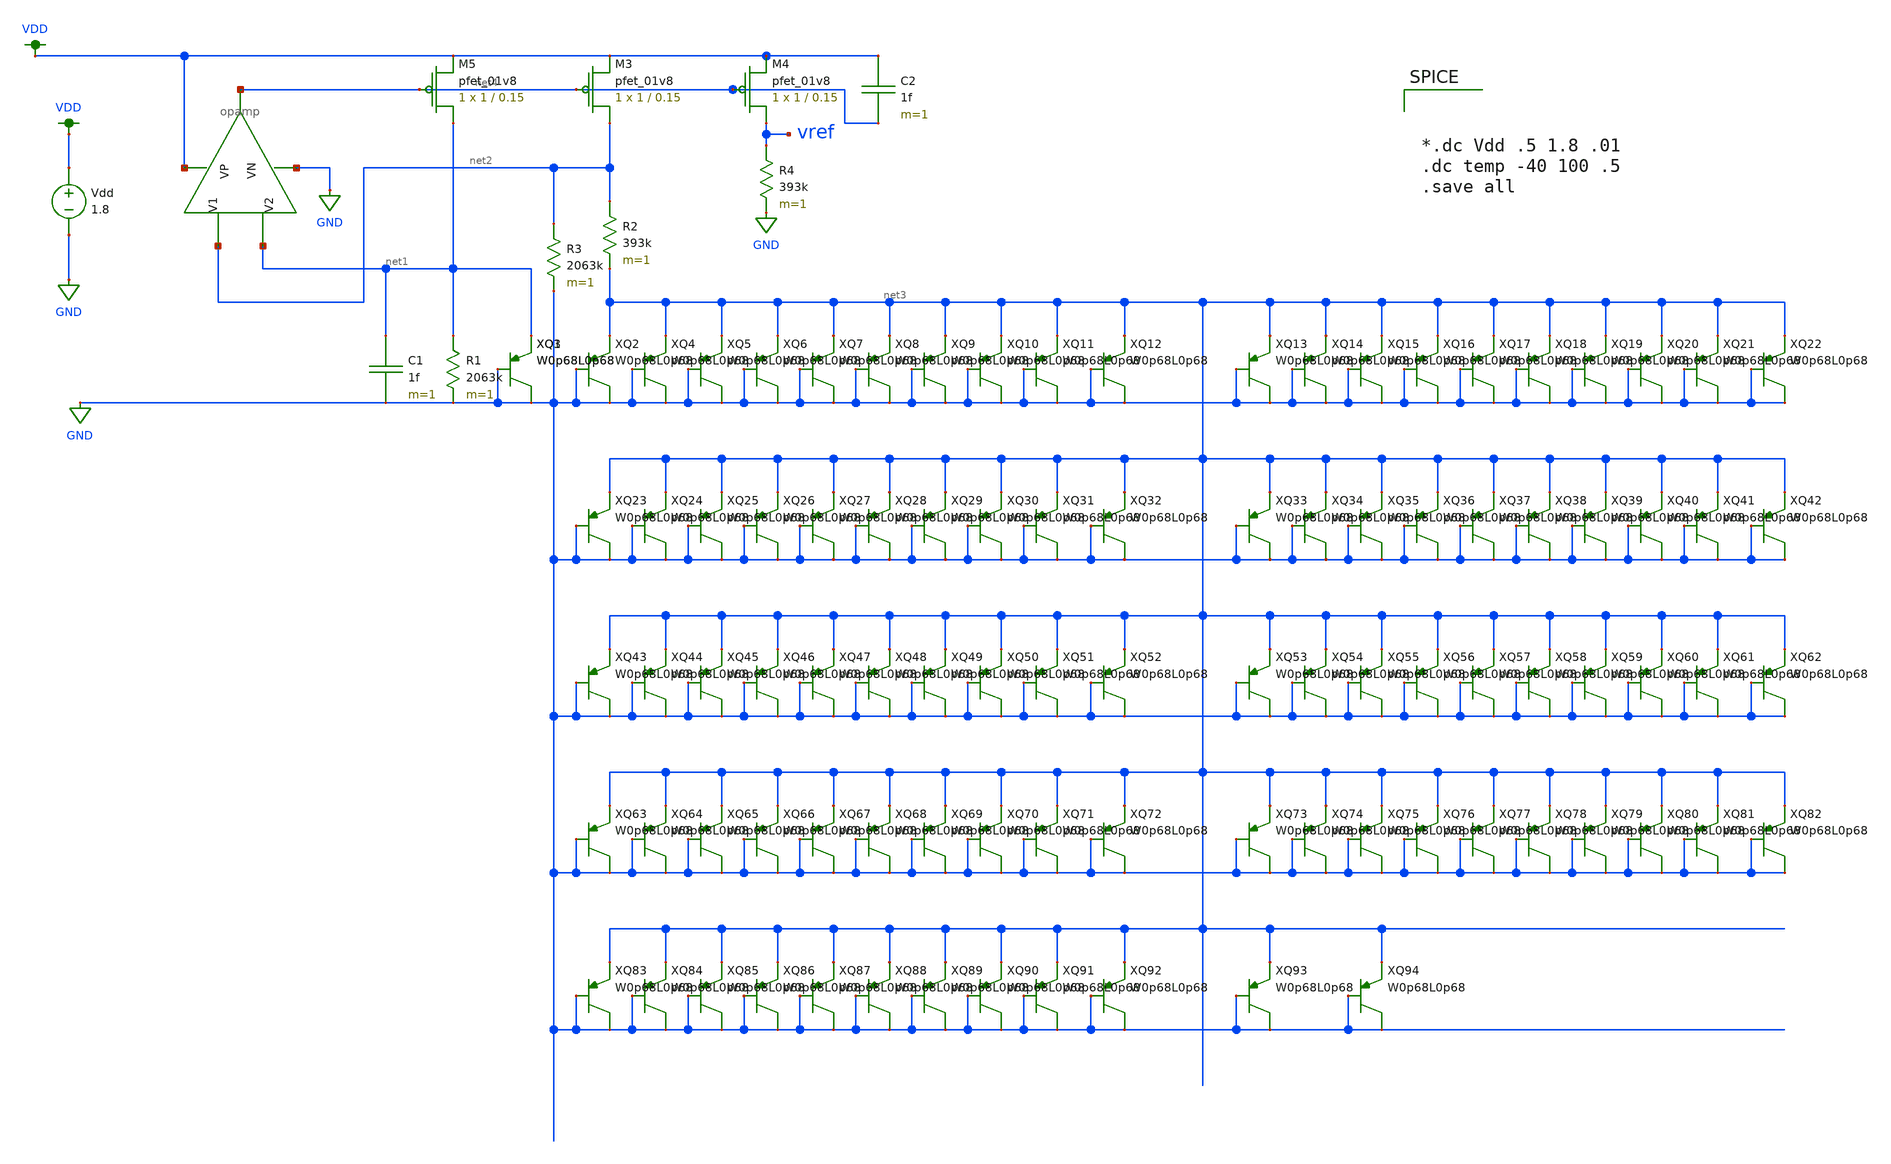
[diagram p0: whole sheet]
** sch_path: schematics/bandgap_pnp.sch
**.subckt bandgap_pnp
XM4 vref net4 VDD VDD sky130_fd_pr__pfet_01v8 L=0.15 W=1 nf=1 ad='int((nf+1)/2) * W/nf * 0.29' as='int((nf+2)/2) * W/nf * 0.29'
+ pd='2*int((nf+1)/2) * (W/nf + 0.29)' ps='2*int((nf+2)/2) * (W/nf + 0.29)' nrd='0.29 / W' nrs='0.29 / W'
+ sa=0 sb=0 sd=0 mult=1 m=1
XM5 net1 net4 VDD VDD sky130_fd_pr__pfet_01v8 L=0.15 W=1 nf=1 ad='int((nf+1)/2) * W/nf * 0.29' as='int((nf+2)/2) * W/nf * 0.29'
+ pd='2*int((nf+1)/2) * (W/nf + 0.29)' ps='2*int((nf+2)/2) * (W/nf + 0.29)' nrd='0.29 / W' nrs='0.29 / W'
+ sa=0 sb=0 sd=0 mult=1 m=1
XM3 net2 net4 VDD VDD sky130_fd_pr__pfet_01v8 L=0.15 W=1 nf=1 ad='int((nf+1)/2) * W/nf * 0.29' as='int((nf+2)/2) * W/nf * 0.29'
+ pd='2*int((nf+1)/2) * (W/nf + 0.29)' ps='2*int((nf+2)/2) * (W/nf + 0.29)' nrd='0.29 / W' nrs='0.29 / W'
+ sa=0 sb=0 sd=0 mult=1 m=1
C1 net1 GND 1f m=1
R1 net1 GND 2063k m=1
R2 net2 net3 393k m=1
R3 net2 GND 2063k m=1
R4 vref GND 393k m=1
C2 VDD net4 1f m=1
Vdd VDD GND 1.8
X1 net2 net1 VDD GND net4 opamp
XQ1 net1 GND GND sky130_fd_pr__pnp_05v0
XQ2 net3 GND GND sky130_fd_pr__pnp_05v0
XQ3 net1 GND GND sky130_fd_pr__pnp_05v0
XQ4 net3 GND GND sky130_fd_pr__pnp_05v0
XQ5 net3 GND GND sky130_fd_pr__pnp_05v0
XQ6 net3 GND GND sky130_fd_pr__pnp_05v0
XQ7 net3 GND GND sky130_fd_pr__pnp_05v0
XQ8 net3 GND GND sky130_fd_pr__pnp_05v0
XQ9 net3 GND GND sky130_fd_pr__pnp_05v0
XQ10 net3 GND GND sky130_fd_pr__pnp_05v0
XQ11 net3 GND GND sky130_fd_pr__pnp_05v0
XQ12 net3 GND GND sky130_fd_pr__pnp_05v0
XQ13 net3 GND GND sky130_fd_pr__pnp_05v0
XQ14 net3 GND GND sky130_fd_pr__pnp_05v0
XQ15 net3 GND GND sky130_fd_pr__pnp_05v0
XQ16 net3 GND GND sky130_fd_pr__pnp_05v0
XQ17 net3 GND GND sky130_fd_pr__pnp_05v0
XQ18 net3 GND GND sky130_fd_pr__pnp_05v0
XQ19 net3 GND GND sky130_fd_pr__pnp_05v0
XQ20 net3 GND GND sky130_fd_pr__pnp_05v0
XQ21 net3 GND GND sky130_fd_pr__pnp_05v0
XQ22 net3 GND GND sky130_fd_pr__pnp_05v0
XQ23 net3 GND GND sky130_fd_pr__pnp_05v0
XQ24 net3 GND GND sky130_fd_pr__pnp_05v0
XQ25 net3 GND GND sky130_fd_pr__pnp_05v0
XQ26 net3 GND GND sky130_fd_pr__pnp_05v0
XQ27 net3 GND GND sky130_fd_pr__pnp_05v0
XQ28 net3 GND GND sky130_fd_pr__pnp_05v0
XQ29 net3 GND GND sky130_fd_pr__pnp_05v0
XQ30 net3 GND GND sky130_fd_pr__pnp_05v0
XQ31 net3 GND GND sky130_fd_pr__pnp_05v0
XQ32 net3 GND GND sky130_fd_pr__pnp_05v0
XQ33 net3 GND GND sky130_fd_pr__pnp_05v0
XQ34 net3 GND GND sky130_fd_pr__pnp_05v0
XQ35 net3 GND GND sky130_fd_pr__pnp_05v0
XQ36 net3 GND GND sky130_fd_pr__pnp_05v0
XQ37 net3 GND GND sky130_fd_pr__pnp_05v0
XQ38 net3 GND GND sky130_fd_pr__pnp_05v0
XQ39 net3 GND GND sky130_fd_pr__pnp_05v0
XQ40 net3 GND GND sky130_fd_pr__pnp_05v0
XQ41 net3 GND GND sky130_fd_pr__pnp_05v0
XQ42 net3 GND GND sky130_fd_pr__pnp_05v0
XQ43 net3 GND GND sky130_fd_pr__pnp_05v0
XQ44 net3 GND GND sky130_fd_pr__pnp_05v0
XQ45 net3 GND GND sky130_fd_pr__pnp_05v0
XQ46 net3 GND GND sky130_fd_pr__pnp_05v0
XQ47 net3 GND GND sky130_fd_pr__pnp_05v0
XQ48 net3 GND GND sky130_fd_pr__pnp_05v0
XQ49 net3 GND GND sky130_fd_pr__pnp_05v0
XQ50 net3 GND GND sky130_fd_pr__pnp_05v0
XQ51 net3 GND GND sky130_fd_pr__pnp_05v0
XQ52 net3 GND GND sky130_fd_pr__pnp_05v0
XQ53 net3 GND GND sky130_fd_pr__pnp_05v0
XQ54 net3 GND GND sky130_fd_pr__pnp_05v0
XQ55 net3 GND GND sky130_fd_pr__pnp_05v0
XQ56 net3 GND GND sky130_fd_pr__pnp_05v0
XQ57 net3 GND GND sky130_fd_pr__pnp_05v0
XQ58 net3 GND GND sky130_fd_pr__pnp_05v0
XQ59 net3 GND GND sky130_fd_pr__pnp_05v0
XQ60 net3 GND GND sky130_fd_pr__pnp_05v0
XQ61 net3 GND GND sky130_fd_pr__pnp_05v0
XQ62 net3 GND GND sky130_fd_pr__pnp_05v0
XQ63 net3 GND GND sky130_fd_pr__pnp_05v0
XQ64 net3 GND GND sky130_fd_pr__pnp_05v0
XQ65 net3 GND GND sky130_fd_pr__pnp_05v0
XQ66 net3 GND GND sky130_fd_pr__pnp_05v0
XQ67 net3 GND GND sky130_fd_pr__pnp_05v0
XQ68 net3 GND GND sky130_fd_pr__pnp_05v0
XQ69 net3 GND GND sky130_fd_pr__pnp_05v0
XQ70 net3 GND GND sky130_fd_pr__pnp_05v0
XQ71 net3 GND GND sky130_fd_pr__pnp_05v0
XQ72 net3 GND GND sky130_fd_pr__pnp_05v0
XQ73 net3 GND GND sky130_fd_pr__pnp_05v0
XQ74 net3 GND GND sky130_fd_pr__pnp_05v0
XQ75 net3 GND GND sky130_fd_pr__pnp_05v0
XQ76 net3 GND GND sky130_fd_pr__pnp_05v0
XQ77 net3 GND GND sky130_fd_pr__pnp_05v0
XQ78 net3 GND GND sky130_fd_pr__pnp_05v0
XQ79 net3 GND GND sky130_fd_pr__pnp_05v0
XQ80 net3 GND GND sky130_fd_pr__pnp_05v0
XQ81 net3 GND GND sky130_fd_pr__pnp_05v0
XQ82 net3 GND GND sky130_fd_pr__pnp_05v0
XQ83 net3 GND GND sky130_fd_pr__pnp_05v0
XQ84 net3 GND GND sky130_fd_pr__pnp_05v0
XQ85 net3 GND GND sky130_fd_pr__pnp_05v0
XQ86 net3 GND GND sky130_fd_pr__pnp_05v0
XQ87 net3 GND GND sky130_fd_pr__pnp_05v0
XQ88 net3 GND GND sky130_fd_pr__pnp_05v0
XQ89 net3 GND GND sky130_fd_pr__pnp_05v0
XQ90 net3 GND GND sky130_fd_pr__pnp_05v0
XQ91 net3 GND GND sky130_fd_pr__pnp_05v0
XQ92 net3 GND GND sky130_fd_pr__pnp_05v0
XQ93 net3 GND GND sky130_fd_pr__pnp_05v0
XQ94 net3 GND GND sky130_fd_pr__pnp_05v0
**** begin user architecture code

.option wnflag=1
.param MC_SWITCH=0.0
.lib ~/skywater/skywater-pdk/libraries/sky130_fd_pr_ngspice/latest/models/sky130.lib.spice tt




*.dc Vdd .5 1.8 .01
.dc temp -40 100 .5
.save all




.subckt sky130_fd_pr__pnp_05v0  E B C
*.iopin E
*.iopin B
*.iopin C
XQ1 C B E C sky130_fd_pr__pnp_05v5_W0p68L0p68
.ends

**** end user architecture code
**.ends

* expanding   symbol:  /home/madvlsi/Desktop/MADVLSI_final/schematics/opamp.sym # of pins=5
** sym_path: schematics/opamp.sym
** sch_path: schematics/opamp.sch
.subckt opamp V1 V2 VP VN Vout
*.ipin V1
*.ipin V2
*.opin Vout
*.iopin VP
*.iopin VN
*.iopin VP
*.iopin VN
XM1 VN net7 net2 GND sky130_fd_pr__nfet_01v8 L=l W=w nf=1 ad='int((nf+1)/2) * W/nf * 0.29' as='int((nf+2)/2) * W/nf * 0.29'
+ pd='2*int((nf+1)/2) * (W/nf + 0.29)' ps='2*int((nf+2)/2) * (W/nf + 0.29)' nrd='0.29 / W' nrs='0.29 / W'
+ sa=0 sb=0 sd=0 mult=1 m=1
XM2 VP net3 net1 VDD sky130_fd_pr__pfet_01v8 L=l W=w nf=1 ad='int((nf+1)/2) * W/nf * 0.29' as='int((nf+2)/2) * W/nf * 0.29'
+ pd='2*int((nf+1)/2) * (W/nf + 0.29)' ps='2*int((nf+2)/2) * (W/nf + 0.29)' nrd='0.29 / W' nrs='0.29 / W'
+ sa=0 sb=0 sd=0 mult=1 m=1
XM3 net1 V1 Vd VDD sky130_fd_pr__pfet_01v8 L=l W=w nf=1 ad='int((nf+1)/2) * W/nf * 0.29' as='int((nf+2)/2) * W/nf * 0.29'
+ pd='2*int((nf+1)/2) * (W/nf + 0.29)' ps='2*int((nf+2)/2) * (W/nf + 0.29)' nrd='0.29 / W' nrs='0.29 / W'
+ sa=0 sb=0 sd=0 mult=1 m=1
XM4 Vc V2 net1 VDD sky130_fd_pr__pfet_01v8 L=l W=w nf=1 ad='int((nf+1)/2) * W/nf * 0.29' as='int((nf+2)/2) * W/nf * 0.29'
+ pd='2*int((nf+1)/2) * (W/nf + 0.29)' ps='2*int((nf+2)/2) * (W/nf + 0.29)' nrd='0.29 / W' nrs='0.29 / W'
+ sa=0 sb=0 sd=0 mult=1 m=1
XM5 Va V2 net2 GND sky130_fd_pr__nfet_01v8 L=l W=w nf=1 ad='int((nf+1)/2) * W/nf * 0.29' as='int((nf+2)/2) * W/nf * 0.29'
+ pd='2*int((nf+1)/2) * (W/nf + 0.29)' ps='2*int((nf+2)/2) * (W/nf + 0.29)' nrd='0.29 / W' nrs='0.29 / W'
+ sa=0 sb=0 sd=0 mult=1 m=1
XM6 net2 V1 Vb GND sky130_fd_pr__nfet_01v8 L=l W=w nf=1 ad='int((nf+1)/2) * W/nf * 0.29' as='int((nf+2)/2) * W/nf * 0.29'
+ pd='2*int((nf+1)/2) * (W/nf + 0.29)' ps='2*int((nf+2)/2) * (W/nf + 0.29)' nrd='0.29 / W' nrs='0.29 / W'
+ sa=0 sb=0 sd=0 mult=1 m=1
XM7 net3 net3 Va VDD sky130_fd_pr__pfet_01v8 L=l W=w nf=1 ad='int((nf+1)/2) * W/nf * 0.29' as='int((nf+2)/2) * W/nf * 0.29'
+ pd='2*int((nf+1)/2) * (W/nf + 0.29)' ps='2*int((nf+2)/2) * (W/nf + 0.29)' nrd='0.29 / W' nrs='0.29 / W'
+ sa=0 sb=0 sd=0 mult=1 m=1
XM8 net6 net6 Va VDD sky130_fd_pr__pfet_01v8 L=l W=w nf=1 ad='int((nf+1)/2) * W/nf * 0.29' as='int((nf+2)/2) * W/nf * 0.29'
+ pd='2*int((nf+1)/2) * (W/nf + 0.29)' ps='2*int((nf+2)/2) * (W/nf + 0.29)' nrd='0.29 / W' nrs='0.29 / W'
+ sa=0 sb=0 sd=0 mult=1 m=1
XM9 net5 net6 Vb VDD sky130_fd_pr__pfet_01v8 L=l W=w nf=1 ad='int((nf+1)/2) * W/nf * 0.29' as='int((nf+2)/2) * W/nf * 0.29'
+ pd='2*int((nf+1)/2) * (W/nf + 0.29)' ps='2*int((nf+2)/2) * (W/nf + 0.29)' nrd='0.29 / W' nrs='0.29 / W'
+ sa=0 sb=0 sd=0 mult=1 m=1
XM10 Va net3 VP VDD sky130_fd_pr__pfet_01v8 L=l W=w nf=1 ad='int((nf+1)/2) * W/nf * 0.29' as='int((nf+2)/2) * W/nf * 0.29'
+ pd='2*int((nf+1)/2) * (W/nf + 0.29)' ps='2*int((nf+2)/2) * (W/nf + 0.29)' nrd='0.29 / W' nrs='0.29 / W'
+ sa=0 sb=0 sd=0 mult=1 m=1
XM11 Vb net3 VP VDD sky130_fd_pr__pfet_01v8 L=l W=w nf=1 ad='int((nf+1)/2) * W/nf * 0.29' as='int((nf+2)/2) * W/nf * 0.29'
+ pd='2*int((nf+1)/2) * (W/nf + 0.29)' ps='2*int((nf+2)/2) * (W/nf + 0.29)' nrd='0.29 / W' nrs='0.29 / W'
+ sa=0 sb=0 sd=0 mult=1 m=1
XM12 net6 net6 Vc GND sky130_fd_pr__nfet_01v8 L=l W=w nf=1 ad='int((nf+1)/2) * W/nf * 0.29' as='int((nf+2)/2) * W/nf * 0.29'
+ pd='2*int((nf+1)/2) * (W/nf + 0.29)' ps='2*int((nf+2)/2) * (W/nf + 0.29)' nrd='0.29 / W' nrs='0.29 / W'
+ sa=0 sb=0 sd=0 mult=1 m=1
XM13 net5 net6 Vd GND sky130_fd_pr__nfet_01v8 L=l W=w nf=1 ad='int((nf+1)/2) * W/nf * 0.29' as='int((nf+2)/2) * W/nf * 0.29'
+ pd='2*int((nf+1)/2) * (W/nf + 0.29)' ps='2*int((nf+2)/2) * (W/nf + 0.29)' nrd='0.29 / W' nrs='0.29 / W'
+ sa=0 sb=0 sd=0 mult=1 m=1
XM14 Vc net7 VN GND sky130_fd_pr__nfet_01v8 L=l W=w nf=1 ad='int((nf+1)/2) * W/nf * 0.29' as='int((nf+2)/2) * W/nf * 0.29'
+ pd='2*int((nf+1)/2) * (W/nf + 0.29)' ps='2*int((nf+2)/2) * (W/nf + 0.29)' nrd='0.29 / W' nrs='0.29 / W'
+ sa=0 sb=0 sd=0 mult=1 m=1
XM15 Vd net7 VN GND sky130_fd_pr__nfet_01v8 L=l W=w nf=1 ad='int((nf+1)/2) * W/nf * 0.29' as='int((nf+2)/2) * W/nf * 0.29'
+ pd='2*int((nf+1)/2) * (W/nf + 0.29)' ps='2*int((nf+2)/2) * (W/nf + 0.29)' nrd='0.29 / W' nrs='0.29 / W'
+ sa=0 sb=0 sd=0 mult=1 m=1
XM16 net8 net7 net3 GND sky130_fd_pr__nfet_01v8 L=l W=w nf=1 ad='int((nf+1)/2) * W/nf * 0.29' as='int((nf+2)/2) * W/nf * 0.29'
+ pd='2*int((nf+1)/2) * (W/nf + 0.29)' ps='2*int((nf+2)/2) * (W/nf + 0.29)' nrd='0.29 / W' nrs='0.29 / W'
+ sa=0 sb=0 sd=0 mult=1 m=1
XM17 VN net7 net8 GND sky130_fd_pr__nfet_01v8 L=l W=w nf=1 ad='int((nf+1)/2) * W/nf * 0.29' as='int((nf+2)/2) * W/nf * 0.29'
+ pd='2*int((nf+1)/2) * (W/nf + 0.29)' ps='2*int((nf+2)/2) * (W/nf + 0.29)' nrd='0.29 / W' nrs='0.29 / W'
+ sa=0 sb=0 sd=0 mult=1 m=1
XM18 net8 net7 VP GND sky130_fd_pr__nfet_01v8 L=l W=w nf=1 ad='int((nf+1)/2) * W/nf * 0.29' as='int((nf+2)/2) * W/nf * 0.29'
+ pd='2*int((nf+1)/2) * (W/nf + 0.29)' ps='2*int((nf+2)/2) * (W/nf + 0.29)' nrd='0.29 / W' nrs='0.29 / W'
+ sa=0 sb=0 sd=0 mult=M m=M
XM19 net4 net3 net7 VDD sky130_fd_pr__pfet_01v8 L=l W=w nf=1 ad='int((nf+1)/2) * W/nf * 0.29' as='int((nf+2)/2) * W/nf * 0.29'
+ pd='2*int((nf+1)/2) * (W/nf + 0.29)' ps='2*int((nf+2)/2) * (W/nf + 0.29)' nrd='0.29 / W' nrs='0.29 / W'
+ sa=0 sb=0 sd=0 mult=1 m=1
XM20 VP net3 net4 VDD sky130_fd_pr__pfet_01v8 L=l W=w nf=1 ad='int((nf+1)/2) * W/nf * 0.29' as='int((nf+2)/2) * W/nf * 0.29'
+ pd='2*int((nf+1)/2) * (W/nf + 0.29)' ps='2*int((nf+2)/2) * (W/nf + 0.29)' nrd='0.29 / W' nrs='0.29 / W'
+ sa=0 sb=0 sd=0 mult=1 m=1
XM21 net4 net3 VN VDD sky130_fd_pr__pfet_01v8 L=l W=w nf=1 ad='int((nf+1)/2) * W/nf * 0.29' as='int((nf+2)/2) * W/nf * 0.29'
+ pd='2*int((nf+1)/2) * (W/nf + 0.29)' ps='2*int((nf+2)/2) * (W/nf + 0.29)' nrd='0.29 / W' nrs='0.29 / W'
+ sa=0 sb=0 sd=0 mult=M m=M
XM22 net7 net7 Vc GND sky130_fd_pr__nfet_01v8 L=l W=w nf=1 ad='int((nf+1)/2) * W/nf * 0.29' as='int((nf+2)/2) * W/nf * 0.29'
+ pd='2*int((nf+1)/2) * (W/nf + 0.29)' ps='2*int((nf+2)/2) * (W/nf + 0.29)' nrd='0.29 / W' nrs='0.29 / W'
+ sa=0 sb=0 sd=0 mult=1 m=1
**** begin user architecture code

.param M=3
.param w=3
.param l=0.6


**** end user architecture code
XM23 Vout net5 VN GND sky130_fd_pr__nfet_01v8 L=.15 W=6 nf=1 ad='int((nf+1)/2) * W/nf * 0.29' as='int((nf+2)/2) * W/nf * 0.29'
+ pd='2*int((nf+1)/2) * (W/nf + 0.29)' ps='2*int((nf+2)/2) * (W/nf + 0.29)' nrd='0.29 / W' nrs='0.29 / W'
+ sa=0 sb=0 sd=0 mult=1 m=1
XM24 Vout net5 VP VDD sky130_fd_pr__pfet_01v8 L=.15 W=12 nf=1 ad='int((nf+1)/2) * W/nf * 0.29' as='int((nf+2)/2) * W/nf * 0.29'
+ pd='2*int((nf+1)/2) * (W/nf + 0.29)' ps='2*int((nf+2)/2) * (W/nf + 0.29)' nrd='0.29 / W' nrs='0.29 / W'
+ sa=0 sb=0 sd=0 mult=1 m=1
C1 Vout net5 500f m=1
.ends

.GLOBAL VDD
.GLOBAL GND
.end
